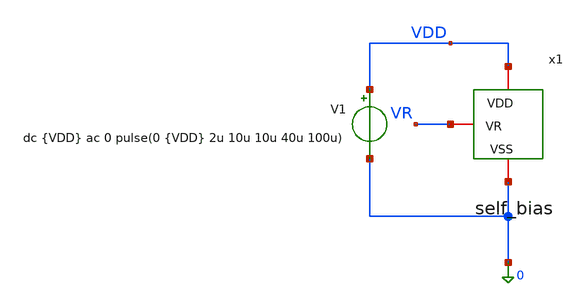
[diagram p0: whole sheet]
** sch_path: xschem/Iref/self_bias_tb.sch
**.subckt self_bias_tb
V1 VDD 0 dc {VDD} ac 0 pulse(0 {VDD} 2u 10u 10u 40u 100u)
x1 VDD VR 0 self_bias
**** begin user architecture code




* 1. Inclusión de libreria de modelos Sky130 PRIMERO
.lib /foss/pdks/sky130A/libs.tech/ngspice/sky130.lib.spice ss
.option temp=-40
.option num_threads=8

**parametros_ldo
.param VDD = 1.62



.param tstart   = 10u
.param trise    = 200u
.param tfall    = 200u

.param tsim = 'tstart+2*trise+tfall'



.control
let tstart   = 10u
let trise    = 200u
let tfall    = 200u

let tsim = '$&tstart+4*$&trise+3*$&tfall'

save all



* Ms2 (pfet_01v8_lvt)
save @m.x1.xMs2.msky130_fd_pr__pfet_01v8_lvt[gm]
save @m.x1.xMs2.msky130_fd_pr__pfet_01v8_lvt[gds]
save @m.x1.xMs2.msky130_fd_pr__pfet_01v8_lvt[id]
save @m.x1.xMs2.msky130_fd_pr__pfet_01v8_lvt[vgs]
save @m.x1.xMs2.msky130_fd_pr__pfet_01v8_lvt[vds]
save @m.x1.xMs2.msky130_fd_pr__pfet_01v8_lvt[vth]
save @m.x1.xMs2.msky130_fd_pr__pfet_01v8_lvt[vdsat]

* Mp3 (pfet_01v8_lvt)
save @m.x1.xMp3.msky130_fd_pr__pfet_01v8_lvt[gm]
save @m.x1.xMp3.msky130_fd_pr__pfet_01v8_lvt[gds]
save @m.x1.xMp3.msky130_fd_pr__pfet_01v8_lvt[id]
save @m.x1.xMp3.msky130_fd_pr__pfet_01v8_lvt[vgs]
save @m.x1.xMp3.msky130_fd_pr__pfet_01v8_lvt[vds]
save @m.x1.xMp3.msky130_fd_pr__pfet_01v8_lvt[vth]
save @m.x1.xMp3.msky130_fd_pr__pfet_01v8_lvt[vdsat]

* Mp4 (pfet_01v8_lvt)
save @m.x1.xMp4.msky130_fd_pr__pfet_01v8_lvt[gm]
save @m.x1.xMp4.msky130_fd_pr__pfet_01v8_lvt[gds]
save @m.x1.xMp4.msky130_fd_pr__pfet_01v8_lvt[id]
save @m.x1.xMp4.msky130_fd_pr__pfet_01v8_lvt[vgs]
save @m.x1.xMp4.msky130_fd_pr__pfet_01v8_lvt[vds]
save @m.x1.xMp4.msky130_fd_pr__pfet_01v8_lvt[vth]
save @m.x1.xMp4.msky130_fd_pr__pfet_01v8_lvt[vdsat]



*Ms1 (nfet_01v8)
save @m.x1.xMs1.msky130_fd_pr__nfet_01v8[gm]
save @m.x1.xMs1.msky130_fd_pr__nfet_01v8[gds]
save @m.x1.xMs1.msky130_fd_pr__nfet_01v8[id]
save @m.x1.xMs1.msky130_fd_pr__nfet_01v8[vgs]
save @m.x1.xMs1.msky130_fd_pr__nfet_01v8[vds]
save @m.x1.xMs1.msky130_fd_pr__nfet_01v8[vth]
save @m.x1.xMs1.msky130_fd_pr__nfet_01v8[vdsat]

*Ms3 (nfet_01v8)
save @m.x1.xMs3.msky130_fd_pr__nfet_01v8[gm]
save @m.x1.xMs3.msky130_fd_pr__nfet_01v8[gds]
save @m.x1.xMs3.msky130_fd_pr__nfet_01v8[id]
save @m.x1.xMs3.msky130_fd_pr__nfet_01v8[vgs]
save @m.x1.xMs3.msky130_fd_pr__nfet_01v8[vds]
save @m.x1.xMs3.msky130_fd_pr__nfet_01v8[vth]
save @m.x1.xMs3.msky130_fd_pr__nfet_01v8[vdsat]

*Mn1 (nfet_01v8)
save @m.x1.xMn1.msky130_fd_pr__nfet_01v8[gm]
save @m.x1.xMn1.msky130_fd_pr__nfet_01v8[gds]
save @m.x1.xMn1.msky130_fd_pr__nfet_01v8[id]
save @m.x1.xMn1.msky130_fd_pr__nfet_01v8[vgs]
save @m.x1.xMn1.msky130_fd_pr__nfet_01v8[vds]
save @m.x1.xMn1.msky130_fd_pr__nfet_01v8[vth]
save @m.x1.xMn1.msky130_fd_pr__nfet_01v8[vdsat]

*Mn2 (nfet_01v8)
save @m.x1.xMn2.msky130_fd_pr__nfet_01v8[gm]
save @m.x1.xMn2.msky130_fd_pr__nfet_01v8[gds]
save @m.x1.xMn2.msky130_fd_pr__nfet_01v8[id]
save @m.x1.xMn2.msky130_fd_pr__nfet_01v8[vgs]
save @m.x1.xMn2.msky130_fd_pr__nfet_01v8[vds]
save @m.x1.xMn2.msky130_fd_pr__nfet_01v8[vth]
save @m.x1.xMn2.msky130_fd_pr__nfet_01v8[vdsat]



set filetype=ascii
op
write self_bias_tb.raw

* 1. Calculamos y guardamos los valores
let vr = v(vr)
let ibias_val_uA_op = '(@m.x1.xMp4.msky130_fd_pr__pfet_01v8_lvt[id])*1000000'


* 2. Imprimimos el texto junto con el valor de la variable
echo VR = $&vr
echo ibias = $&ibias_val_uA_op

tran 2u 300u

meas tran vr_tan FIND v(vr) at=30u


let vr_tran = 'vr_tan'

echo vr_tran = $&vr_tran
.endc



**** end user architecture code
**.ends

* expanding   symbol:  self_bias.sym # of pins=3
** sym_path: xschem/Iref/self_bias.sym
** sch_path: xschem/Iref/self_bias.sch
.subckt self_bias VDD VR VSS
*.iopin VR
*.iopin VDD
*.iopin VSS
XMp4 Vgp Vgp VDD VDD sky130_fd_pr__pfet_01v8_lvt L=1 W=30 nf=1 ad='int((1 + 1)/2) * 30 / 1 * 0.29' as='int((1 + 2)/2) * 30 / 1 * 0.29'
+ pd='2*int((1 + 1)/2) * (30 / 1 + 0.29)' ps='2*int((1 + 2)/2) * (30 / 1 + 0.29)' nrd='0.29 / 30 ' nrs='0.29 / 30 '
+ sa=0 sb=0 sd=0 mult=1 m=1
XMp3 VDI Vgp VDD VDD sky130_fd_pr__pfet_01v8_lvt L=1 W=30 nf=1 ad='int((1 + 1)/2) * 30 / 1 * 0.29' as='int((1 + 2)/2) * 30 / 1 * 0.29'
+ pd='2*int((1 + 1)/2) * (30 / 1 + 0.29)' ps='2*int((1 + 2)/2) * (30 / 1 + 0.29)' nrd='0.29 / 30 ' nrs='0.29 / 30 '
+ sa=0 sb=0 sd=0 mult=1 m=1
XMs2 VDinv VR VDD VDD sky130_fd_pr__pfet_01v8_lvt L=25 W=0.5 nf=1 ad='int((1 + 1)/2) * 0.5 / 1 * 0.29'
+ as='int((1 + 2)/2) * 0.5 / 1 * 0.29' pd='2*int((1 + 1)/2) * (0.5 / 1 + 0.29)' ps='2*int((1 + 2)/2) * (0.5 / 1 + 0.29)'
+ nrd='0.29 / 0.5 ' nrs='0.29 / 0.5 ' sa=0 sb=0 sd=0 mult=1 m=1
XR4 VSS VR VSS sky130_fd_pr__res_iso_pw W=0.7 L=11 m=1
XMn2 Vgp VDI VR VSS sky130_fd_pr__nfet_01v8 L=1 W=20 nf=1 ad='int((1 + 1)/2) * 20 / 1 * 0.29' as='int((1 + 2)/2) * 20 / 1 * 0.29'
+ pd='2*int((1 + 1)/2) * (20 / 1 + 0.29)' ps='2*int((1 + 2)/2) * (20 / 1 + 0.29)' nrd='0.29 / 20 ' nrs='0.29 / 20 '
+ sa=0 sb=0 sd=0 mult=1 m=1
XMn1 VDI VR VSS VSS sky130_fd_pr__nfet_01v8 L=1 W=5 nf=1 ad='int((1 + 1)/2) * 5 / 1 * 0.29' as='int((1 + 2)/2) * 5 / 1 * 0.29'
+ pd='2*int((1 + 1)/2) * (5 / 1 + 0.29)' ps='2*int((1 + 2)/2) * (5 / 1 + 0.29)' nrd='0.29 / 5 ' nrs='0.29 / 5 '
+ sa=0 sb=0 sd=0 mult=1 m=1
XMs3 VDinv VR VSS VSS sky130_fd_pr__nfet_01v8 L=1 W=20 nf=1 ad='int((1 + 1)/2) * 20 / 1 * 0.29' as='int((1 + 2)/2) * 20 / 1 * 0.29'
+ pd='2*int((1 + 1)/2) * (20 / 1 + 0.29)' ps='2*int((1 + 2)/2) * (20 / 1 + 0.29)' nrd='0.29 / 20 ' nrs='0.29 / 20 '
+ sa=0 sb=0 sd=0 mult=1 m=1
XMs1 Vgp VDinv VSS VSS sky130_fd_pr__nfet_01v8 L=1 W=2 nf=1 ad='int((1 + 1)/2) * 2 / 1 * 0.29' as='int((1 + 2)/2) * 2 / 1 * 0.29'
+ pd='2*int((1 + 1)/2) * (2 / 1 + 0.29)' ps='2*int((1 + 2)/2) * (2 / 1 + 0.29)' nrd='0.29 / 2 ' nrs='0.29 / 2 '
+ sa=0 sb=0 sd=0 mult=1 m=1
.ends

.end
